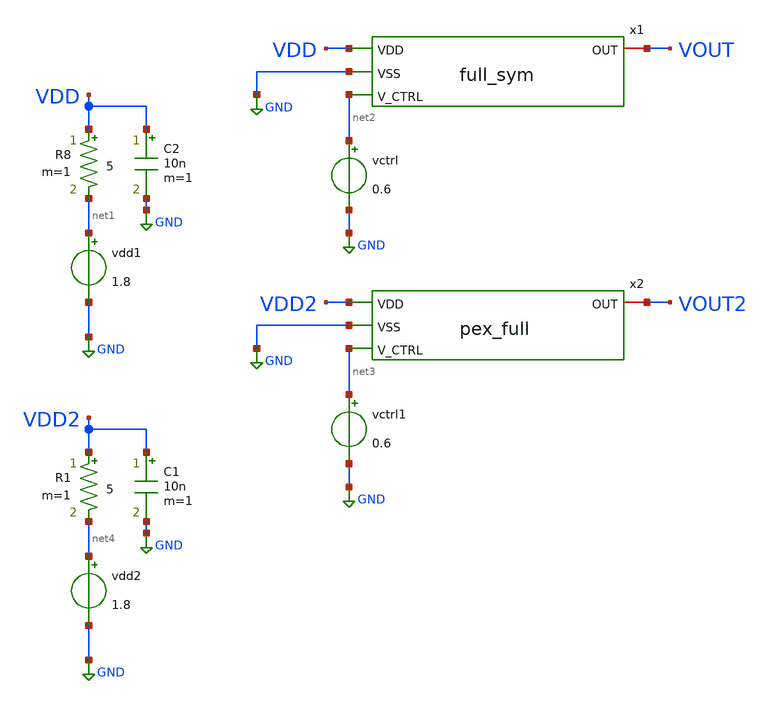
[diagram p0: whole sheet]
** sch_path: schem/sym_full_tb.sch
**.subckt sym_full_tb
vdd1 net1 GND 1.8
C2 VDD GND 10n m=1
R8 VDD net1 5 m=1
vctrl net2 GND 0.6
vctrl1 net3 GND 0.6
vdd2 net4 GND 1.8
C1 VDD2 GND 10n m=1
R1 VDD2 net4 5 m=1
x1 VDD GND VOUT net2 full_sym
x2 VDD2 GND VOUT2 net3 vco_pex
**** begin user architecture code



.include /home/zhixuan/projects/fyp_vco/magic/full/vco_pex.spice
.lib /usr/local/share/pdk/sky130A/libs.tech/ngspice/sky130.lib.spice tt

.tran 0.1n 2u
.save all

.control
    run

    meas tran t11 when VOUT=0.9 rise=2
    meas tran t21 when VOUT=0.9 rise=3

    meas tran t12 when VOUT2=0.9 rise=2
    meas tran t22 when VOUT2=0.9 rise=3

    * Calculate period and frequency from 2nd period onwards
    let period1 = t21 - t11
    let period2 = t22 - t12

    let freq1 = 1 / period1
    let freq2 = 1 / period2

    print period1
    print freq1
    print period2
    print freq2

    plot VOUT2 v(x2.comp_p_0/VIN_N)
    plot abs(i(vdd2))*1.8
    plot abs(i(vdd1))*1.8

    * echo "VOUT2 v(x2.comp_p_0/VIN_N)" > /home/zhixuan/projects/fyp_vco/schem/full_out1.txt
    * print col VOUT2 v(x2.comp_p_0/VIN_N) >> /home/zhixuan/projects/fyp_vco/schem/full_out1.txt
.endc

.end


**** end user architecture code
**.ends

* expanding   symbol:  /home/zhixuan/projects/fyp_vco/schem/full_sym.sym # of pins=4
** sym_path: schem/full_sym.sym
** sch_path: schem/full_sym.sch
.subckt full_sym VDD VSS OUT V_CTRL
*.ipin VDD
*.ipin VSS
*.iopin OUT
*.ipin V_CTRL
x1 VDD VSS high v_cap comp_n bias_n sym_comp_n
x2 VDD VSS bias_p comp_p V_CTRL v_cap sym_comp_p
x5 VDD feedback net4 VSS sym_inv
x7 VDD VSS comp_p comp_n feedback net5 sym_sr_latch
XC1 v_cap VSS sky130_fd_pr__cap_mim_m3_1 W=20 L=20 MF=1 m=1
XM33 net1 feedback VSS VSS sky130_fd_pr__nfet_01v8 L=0.3 W=2 nf=5 ad='int((5 + 1)/2) * 2 / 5 * 0.29'
+ as='int((5 + 2)/2) * 2 / 5 * 0.29' pd='2*int((5 + 1)/2) * (2 / 5 + 0.29)' ps='2*int((5 + 2)/2) * (2 / 5 + 0.29)'
+ nrd='0.29 / 2 ' nrs='0.29 / 2 ' sa=0 sb=0 sd=0 mult=1 m=1
XM34 net1 feedback VDD VDD sky130_fd_pr__pfet_01v8 L=0.3 W=2 nf=10 ad='int((10 + 1)/2) * 2 / 10 * 0.29'
+ as='int((10 + 2)/2) * 2 / 10 * 0.29' pd='2*int((10 + 1)/2) * (2 / 10 + 0.29)' ps='2*int((10 + 2)/2) * (2 / 10 + 0.29)'
+ nrd='0.29 / 2 ' nrs='0.29 / 2 ' sa=0 sb=0 sd=0 mult=1 m=1
XR1 v_cap net1 VSS sky130_fd_pr__res_xhigh_po_0p35 L=15 mult=1 m=1
x3 VDD VSS net2 net3 high bias_n sym_opamp
XR2 net2 VDD VSS sky130_fd_pr__res_xhigh_po_0p35 L=24 mult=1 m=1
XR3 VSS net2 VSS sky130_fd_pr__res_xhigh_po_0p35 L=24 mult=1 m=1
XR4 V_CTRL net3 VSS sky130_fd_pr__res_xhigh_po_0p35 L=24 mult=1 m=1
XR5 net3 high VSS sky130_fd_pr__res_xhigh_po_0p35 L=24 mult=1 m=1
XM2 OUT net4 VSS VSS sky130_fd_pr__nfet_01v8 L=0.3 W=2 nf=2 ad='int((2 + 1)/2) * 2 / 2 * 0.29' as='int((2 + 2)/2) * 2 / 2 * 0.29'
+ pd='2*int((2 + 1)/2) * (2 / 2 + 0.29)' ps='2*int((2 + 2)/2) * (2 / 2 + 0.29)' nrd='0.29 / 2 ' nrs='0.29 / 2 '
+ sa=0 sb=0 sd=0 mult=1 m=1
XM4 OUT net4 VDD VDD sky130_fd_pr__pfet_01v8 L=0.3 W=2 nf=4 ad='int((4 + 1)/2) * 2 / 4 * 0.29' as='int((4 + 2)/2) * 2 / 4 * 0.29'
+ pd='2*int((4 + 1)/2) * (2 / 4 + 0.29)' ps='2*int((4 + 2)/2) * (2 / 4 + 0.29)' nrd='0.29 / 2 ' nrs='0.29 / 2 '
+ sa=0 sb=0 sd=0 mult=1 m=1
x4 VDD VSS bias_p bias_n sym_ptat
.ends


* expanding   symbol:  /home/zhixuan/projects/fyp_vco/schem/symbol_repo/sym_comp_n.sym # of pins=6
** sym_path: schem/symbol_repo/sym_comp_n.sym
** sch_path: schem/symbol_repo/sym_comp_n.sch
.subckt sym_comp_n VDD VSS VIN_N VIN_P VOUT BIAS_N
*.ipin VDD
*.ipin VSS
*.ipin VIN_N
*.ipin VIN_P
*.ipin BIAS_N
*.iopin VOUT
XMP_diode_l net1 net1 VDD VDD sky130_fd_pr__pfet_01v8 L=0.3 W=2 nf=2 ad='int((2 + 1)/2) * 2 / 2 * 0.29'
+ as='int((2 + 2)/2) * 2 / 2 * 0.29' pd='2*int((2 + 1)/2) * (2 / 2 + 0.29)' ps='2*int((2 + 2)/2) * (2 / 2 + 0.29)'
+ nrd='0.29 / 2 ' nrs='0.29 / 2 ' sa=0 sb=0 sd=0 mult=1 m=1
XMP_cs_l net2 net1 VDD VDD sky130_fd_pr__pfet_01v8 L=0.3 W=2 nf=2 ad='int((2 + 1)/2) * 2 / 2 * 0.29'
+ as='int((2 + 2)/2) * 2 / 2 * 0.29' pd='2*int((2 + 1)/2) * (2 / 2 + 0.29)' ps='2*int((2 + 2)/2) * (2 / 2 + 0.29)'
+ nrd='0.29 / 2 ' nrs='0.29 / 2 ' sa=0 sb=0 sd=0 mult=1 m=1
XMP_cs_r net1 net2 VDD VDD sky130_fd_pr__pfet_01v8 L=0.3 W=2 nf=2 ad='int((2 + 1)/2) * 2 / 2 * 0.29'
+ as='int((2 + 2)/2) * 2 / 2 * 0.29' pd='2*int((2 + 1)/2) * (2 / 2 + 0.29)' ps='2*int((2 + 2)/2) * (2 / 2 + 0.29)'
+ nrd='0.29 / 2 ' nrs='0.29 / 2 ' sa=0 sb=0 sd=0 mult=1 m=1
XMP_diode_r net2 net2 VDD VDD sky130_fd_pr__pfet_01v8 L=0.3 W=2 nf=2 ad='int((2 + 1)/2) * 2 / 2 * 0.29'
+ as='int((2 + 2)/2) * 2 / 2 * 0.29' pd='2*int((2 + 1)/2) * (2 / 2 + 0.29)' ps='2*int((2 + 2)/2) * (2 / 2 + 0.29)'
+ nrd='0.29 / 2 ' nrs='0.29 / 2 ' sa=0 sb=0 sd=0 mult=1 m=1
XMN_vinn net1 VIN_N net3 VSS sky130_fd_pr__nfet_01v8 L=0.5 W=2.5 nf=1 ad='int((1 + 1)/2) * 2.5 / 1 * 0.29'
+ as='int((1 + 2)/2) * 2.5 / 1 * 0.29' pd='2*int((1 + 1)/2) * (2.5 / 1 + 0.29)' ps='2*int((1 + 2)/2) * (2.5 / 1 + 0.29)'
+ nrd='0.29 / 2.5 ' nrs='0.29 / 2.5 ' sa=0 sb=0 sd=0 mult=1 m=1
XMN_vinp net2 VIN_P net3 VSS sky130_fd_pr__nfet_01v8 L=0.5 W=2.5 nf=1 ad='int((1 + 1)/2) * 2.5 / 1 * 0.29'
+ as='int((1 + 2)/2) * 2.5 / 1 * 0.29' pd='2*int((1 + 1)/2) * (2.5 / 1 + 0.29)' ps='2*int((1 + 2)/2) * (2.5 / 1 + 0.29)'
+ nrd='0.29 / 2.5 ' nrs='0.29 / 2.5 ' sa=0 sb=0 sd=0 mult=1 m=1
XMN_tail net3 BIAS_N VSS VSS sky130_fd_pr__nfet_01v8 L=0.75 W=2.5 nf=2 ad='int((2 + 1)/2) * 2.5 / 2 * 0.29'
+ as='int((2 + 2)/2) * 2.5 / 2 * 0.29' pd='2*int((2 + 1)/2) * (2.5 / 2 + 0.29)' ps='2*int((2 + 2)/2) * (2.5 / 2 + 0.29)'
+ nrd='0.29 / 2.5 ' nrs='0.29 / 2.5 ' sa=0 sb=0 sd=0 mult=1 m=1
XMP_latch_r VOUT net2 VDD VDD sky130_fd_pr__pfet_01v8 L=0.15 W=0.5 nf=1 ad='int((1 + 1)/2) * 0.5 / 1 * 0.29'
+ as='int((1 + 2)/2) * 0.5 / 1 * 0.29' pd='2*int((1 + 1)/2) * (0.5 / 1 + 0.29)' ps='2*int((1 + 2)/2) * (0.5 / 1 + 0.29)'
+ nrd='0.29 / 0.5 ' nrs='0.29 / 0.5 ' sa=0 sb=0 sd=0 mult=1 m=1
XMP_latch_l net5 net1 VDD VDD sky130_fd_pr__pfet_01v8 L=0.15 W=0.5 nf=1 ad='int((1 + 1)/2) * 0.5 / 1 * 0.29'
+ as='int((1 + 2)/2) * 0.5 / 1 * 0.29' pd='2*int((1 + 1)/2) * (0.5 / 1 + 0.29)' ps='2*int((1 + 2)/2) * (0.5 / 1 + 0.29)'
+ nrd='0.29 / 0.5 ' nrs='0.29 / 0.5 ' sa=0 sb=0 sd=0 mult=1 m=1
XMN_latch_r VOUT net4 VSS VSS sky130_fd_pr__nfet_01v8 L=0.15 W=0.5 nf=1 ad='int((1 + 1)/2) * 0.5 / 1 * 0.29'
+ as='int((1 + 2)/2) * 0.5 / 1 * 0.29' pd='2*int((1 + 1)/2) * (0.5 / 1 + 0.29)' ps='2*int((1 + 2)/2) * (0.5 / 1 + 0.29)'
+ nrd='0.29 / 0.5 ' nrs='0.29 / 0.5 ' sa=0 sb=0 sd=0 mult=1 m=1
XMN_diode_l net4 net4 VSS VSS sky130_fd_pr__nfet_01v8 L=0.15 W=0.5 nf=1 ad='int((1 + 1)/2) * 0.5 / 1 * 0.29'
+ as='int((1 + 2)/2) * 0.5 / 1 * 0.29' pd='2*int((1 + 1)/2) * (0.5 / 1 + 0.29)' ps='2*int((1 + 2)/2) * (0.5 / 1 + 0.29)'
+ nrd='0.29 / 0.5 ' nrs='0.29 / 0.5 ' sa=0 sb=0 sd=0 mult=1 m=1
XMP_lim net4 net4 net5 VDD sky130_fd_pr__pfet_01v8 L=0.15 W=0.5 nf=1 ad='int((1 + 1)/2) * 0.5 / 1 * 0.29'
+ as='int((1 + 2)/2) * 0.5 / 1 * 0.29' pd='2*int((1 + 1)/2) * (0.5 / 1 + 0.29)' ps='2*int((1 + 2)/2) * (0.5 / 1 + 0.29)'
+ nrd='0.29 / 0.5 ' nrs='0.29 / 0.5 ' sa=0 sb=0 sd=0 mult=1 m=1
.ends


* expanding   symbol:  /home/zhixuan/projects/fyp_vco/schem/symbol_repo/sym_comp_p.sym # of pins=6
** sym_path: schem/symbol_repo/sym_comp_p.sym
** sch_path: schem/symbol_repo/sym_comp_p.sch
.subckt sym_comp_p VDD VSS BIAS_P VOUT VIN_P VIN_N
*.ipin VDD
*.ipin VSS
*.ipin BIAS_P
*.ipin VIN_N
*.ipin VIN_P
*.iopin VOUT
XMN_cs_l net2 net1 VSS VSS sky130_fd_pr__nfet_01v8 L=0.15 W=1 nf=1 ad='int((1 + 1)/2) * 1 / 1 * 0.29'
+ as='int((1 + 2)/2) * 1 / 1 * 0.29' pd='2*int((1 + 1)/2) * (1 / 1 + 0.29)' ps='2*int((1 + 2)/2) * (1 / 1 + 0.29)'
+ nrd='0.29 / 1 ' nrs='0.29 / 1 ' sa=0 sb=0 sd=0 mult=1 m=1
XMP_tail net4 BIAS_P VDD VDD sky130_fd_pr__pfet_01v8 L=0.75 W=2 nf=5 ad='int((5 + 1)/2) * 2 / 5 * 0.29'
+ as='int((5 + 2)/2) * 2 / 5 * 0.29' pd='2*int((5 + 1)/2) * (2 / 5 + 0.29)' ps='2*int((5 + 2)/2) * (2 / 5 + 0.29)'
+ nrd='0.29 / 2 ' nrs='0.29 / 2 ' sa=0 sb=0 sd=0 mult=1 m=1
XMP_vinn net1 VIN_N net4 VDD sky130_fd_pr__pfet_01v8 L=0.5 W=2.5 nf=2 ad='int((2 + 1)/2) * 2.5 / 2 * 0.29'
+ as='int((2 + 2)/2) * 2.5 / 2 * 0.29' pd='2*int((2 + 1)/2) * (2.5 / 2 + 0.29)' ps='2*int((2 + 2)/2) * (2.5 / 2 + 0.29)'
+ nrd='0.29 / 2.5 ' nrs='0.29 / 2.5 ' sa=0 sb=0 sd=0 mult=1 m=1
XMP_vinp net2 VIN_P net4 VDD sky130_fd_pr__pfet_01v8 L=0.5 W=2.5 nf=2 ad='int((2 + 1)/2) * 2.5 / 2 * 0.29'
+ as='int((2 + 2)/2) * 2.5 / 2 * 0.29' pd='2*int((2 + 1)/2) * (2.5 / 2 + 0.29)' ps='2*int((2 + 2)/2) * (2.5 / 2 + 0.29)'
+ nrd='0.29 / 2.5 ' nrs='0.29 / 2.5 ' sa=0 sb=0 sd=0 mult=1 m=1
XMN_diode_l net1 net1 VSS VSS sky130_fd_pr__nfet_01v8 L=0.15 W=1 nf=1 ad='int((1 + 1)/2) * 1 / 1 * 0.29'
+ as='int((1 + 2)/2) * 1 / 1 * 0.29' pd='2*int((1 + 1)/2) * (1 / 1 + 0.29)' ps='2*int((1 + 2)/2) * (1 / 1 + 0.29)'
+ nrd='0.29 / 1 ' nrs='0.29 / 1 ' sa=0 sb=0 sd=0 mult=1 m=1
XMN_diode_r net2 net2 VSS VSS sky130_fd_pr__nfet_01v8 L=0.15 W=1 nf=1 ad='int((1 + 1)/2) * 1 / 1 * 0.29'
+ as='int((1 + 2)/2) * 1 / 1 * 0.29' pd='2*int((1 + 1)/2) * (1 / 1 + 0.29)' ps='2*int((1 + 2)/2) * (1 / 1 + 0.29)'
+ nrd='0.29 / 1 ' nrs='0.29 / 1 ' sa=0 sb=0 sd=0 mult=1 m=1
XMN_cs_r net1 net2 VSS VSS sky130_fd_pr__nfet_01v8 L=0.15 W=1 nf=1 ad='int((1 + 1)/2) * 1 / 1 * 0.29'
+ as='int((1 + 2)/2) * 1 / 1 * 0.29' pd='2*int((1 + 1)/2) * (1 / 1 + 0.29)' ps='2*int((1 + 2)/2) * (1 / 1 + 0.29)'
+ nrd='0.29 / 1 ' nrs='0.29 / 1 ' sa=0 sb=0 sd=0 mult=1 m=1
XMN_latch_l net5 net1 VSS VSS sky130_fd_pr__nfet_01v8 L=0.15 W=0.5 nf=1 ad='int((1 + 1)/2) * 0.5 / 1 * 0.29'
+ as='int((1 + 2)/2) * 0.5 / 1 * 0.29' pd='2*int((1 + 1)/2) * (0.5 / 1 + 0.29)' ps='2*int((1 + 2)/2) * (0.5 / 1 + 0.29)'
+ nrd='0.29 / 0.5 ' nrs='0.29 / 0.5 ' sa=0 sb=0 sd=0 mult=1 m=1
XMN_latch_r VOUT net2 VSS VSS sky130_fd_pr__nfet_01v8 L=0.15 W=0.5 nf=1 ad='int((1 + 1)/2) * 0.5 / 1 * 0.29'
+ as='int((1 + 2)/2) * 0.5 / 1 * 0.29' pd='2*int((1 + 1)/2) * (0.5 / 1 + 0.29)' ps='2*int((1 + 2)/2) * (0.5 / 1 + 0.29)'
+ nrd='0.29 / 0.5 ' nrs='0.29 / 0.5 ' sa=0 sb=0 sd=0 mult=1 m=1
XMP_diode_l net3 net3 VDD VDD sky130_fd_pr__pfet_01v8 L=0.15 W=0.5 nf=1 ad='int((1 + 1)/2) * 0.5 / 1 * 0.29'
+ as='int((1 + 2)/2) * 0.5 / 1 * 0.29' pd='2*int((1 + 1)/2) * (0.5 / 1 + 0.29)' ps='2*int((1 + 2)/2) * (0.5 / 1 + 0.29)'
+ nrd='0.29 / 0.5 ' nrs='0.29 / 0.5 ' sa=0 sb=0 sd=0 mult=1 m=1
XMP_latch_r VOUT net3 VDD VDD sky130_fd_pr__pfet_01v8 L=0.15 W=0.5 nf=1 ad='int((1 + 1)/2) * 0.5 / 1 * 0.29'
+ as='int((1 + 2)/2) * 0.5 / 1 * 0.29' pd='2*int((1 + 1)/2) * (0.5 / 1 + 0.29)' ps='2*int((1 + 2)/2) * (0.5 / 1 + 0.29)'
+ nrd='0.29 / 0.5 ' nrs='0.29 / 0.5 ' sa=0 sb=0 sd=0 mult=1 m=1
XMP_lim net5 net5 net3 VDD sky130_fd_pr__pfet_01v8 L=0.15 W=0.5 nf=1 ad='int((1 + 1)/2) * 0.5 / 1 * 0.29'
+ as='int((1 + 2)/2) * 0.5 / 1 * 0.29' pd='2*int((1 + 1)/2) * (0.5 / 1 + 0.29)' ps='2*int((1 + 2)/2) * (0.5 / 1 + 0.29)'
+ nrd='0.29 / 0.5 ' nrs='0.29 / 0.5 ' sa=0 sb=0 sd=0 mult=1 m=1
.ends


* expanding   symbol:  /home/zhixuan/projects/fyp_vco/schem/symbol_repo/sym_inv.sym # of pins=4
** sym_path: schem/symbol_repo/sym_inv.sym
** sch_path: schem/symbol_repo/sym_inv.sch
.subckt sym_inv VDD VIN VOUT VSS
*.ipin VIN
*.ipin VDD
*.ipin VSS
*.iopin VOUT
XMN_pldwn VOUT VIN VSS VSS sky130_fd_pr__nfet_01v8 L=0.15 W=1 nf=1 ad='int((1 + 1)/2) * 1 / 1 * 0.29'
+ as='int((1 + 2)/2) * 1 / 1 * 0.29' pd='2*int((1 + 1)/2) * (1 / 1 + 0.29)' ps='2*int((1 + 2)/2) * (1 / 1 + 0.29)'
+ nrd='0.29 / 1 ' nrs='0.29 / 1 ' sa=0 sb=0 sd=0 mult=1 m=1
XMP_plup VOUT VIN VDD VDD sky130_fd_pr__pfet_01v8 L=0.15 W=2 nf=1 ad='int((1 + 1)/2) * 2 / 1 * 0.29'
+ as='int((1 + 2)/2) * 2 / 1 * 0.29' pd='2*int((1 + 1)/2) * (2 / 1 + 0.29)' ps='2*int((1 + 2)/2) * (2 / 1 + 0.29)'
+ nrd='0.29 / 2 ' nrs='0.29 / 2 ' sa=0 sb=0 sd=0 mult=1 m=1
.ends


* expanding   symbol:  /home/zhixuan/projects/fyp_vco/schem/symbol_repo/sym_sr_latch.sym # of pins=6
** sym_path: schem/symbol_repo/sym_sr_latch.sym
** sch_path: schem/symbol_repo/sym_sr_latch.sch
.subckt sym_sr_latch VDD VSS R S NEG POS
*.ipin S
*.ipin VDD
*.ipin R
*.ipin VSS
*.iopin POS
*.iopin NEG
XMN_neg POS NEG VSS VSS sky130_fd_pr__nfet_01v8 L=0.15 W=1 nf=1 ad='int((1 + 1)/2) * 1 / 1 * 0.29' as='int((1 + 2)/2) * 1 / 1 * 0.29'
+ pd='2*int((1 + 1)/2) * (1 / 1 + 0.29)' ps='2*int((1 + 2)/2) * (1 / 1 + 0.29)' nrd='0.29 / 1 ' nrs='0.29 / 1 '
+ sa=0 sb=0 sd=0 mult=1 m=1
XMP_s net1 S VDD VDD sky130_fd_pr__pfet_01v8 L=0.15 W=2 nf=1 ad='int((1 + 1)/2) * 2 / 1 * 0.29' as='int((1 + 2)/2) * 2 / 1 * 0.29'
+ pd='2*int((1 + 1)/2) * (2 / 1 + 0.29)' ps='2*int((1 + 2)/2) * (2 / 1 + 0.29)' nrd='0.29 / 2 ' nrs='0.29 / 2 '
+ sa=0 sb=0 sd=0 mult=1 m=1
XMP_neg POS NEG net1 VDD sky130_fd_pr__pfet_01v8 L=0.15 W=2 nf=1 ad='int((1 + 1)/2) * 2 / 1 * 0.29' as='int((1 + 2)/2) * 2 / 1 * 0.29'
+ pd='2*int((1 + 1)/2) * (2 / 1 + 0.29)' ps='2*int((1 + 2)/2) * (2 / 1 + 0.29)' nrd='0.29 / 2 ' nrs='0.29 / 2 '
+ sa=0 sb=0 sd=0 mult=1 m=1
XMN_s POS S VSS VSS sky130_fd_pr__nfet_01v8 L=0.15 W=1 nf=1 ad='int((1 + 1)/2) * 1 / 1 * 0.29' as='int((1 + 2)/2) * 1 / 1 * 0.29'
+ pd='2*int((1 + 1)/2) * (1 / 1 + 0.29)' ps='2*int((1 + 2)/2) * (1 / 1 + 0.29)' nrd='0.29 / 1 ' nrs='0.29 / 1 '
+ sa=0 sb=0 sd=0 mult=1 m=1
XMN_r NEG R VSS VSS sky130_fd_pr__nfet_01v8 L=0.15 W=1 nf=1 ad='int((1 + 1)/2) * 1 / 1 * 0.29' as='int((1 + 2)/2) * 1 / 1 * 0.29'
+ pd='2*int((1 + 1)/2) * (1 / 1 + 0.29)' ps='2*int((1 + 2)/2) * (1 / 1 + 0.29)' nrd='0.29 / 1 ' nrs='0.29 / 1 '
+ sa=0 sb=0 sd=0 mult=1 m=1
XMP_r net2 R VDD VDD sky130_fd_pr__pfet_01v8 L=0.15 W=2 nf=1 ad='int((1 + 1)/2) * 2 / 1 * 0.29' as='int((1 + 2)/2) * 2 / 1 * 0.29'
+ pd='2*int((1 + 1)/2) * (2 / 1 + 0.29)' ps='2*int((1 + 2)/2) * (2 / 1 + 0.29)' nrd='0.29 / 2 ' nrs='0.29 / 2 '
+ sa=0 sb=0 sd=0 mult=1 m=1
XMP_pos NEG POS net2 VDD sky130_fd_pr__pfet_01v8 L=0.15 W=2 nf=1 ad='int((1 + 1)/2) * 2 / 1 * 0.29' as='int((1 + 2)/2) * 2 / 1 * 0.29'
+ pd='2*int((1 + 1)/2) * (2 / 1 + 0.29)' ps='2*int((1 + 2)/2) * (2 / 1 + 0.29)' nrd='0.29 / 2 ' nrs='0.29 / 2 '
+ sa=0 sb=0 sd=0 mult=1 m=1
XMN_pos NEG POS VSS VSS sky130_fd_pr__nfet_01v8 L=0.15 W=1 nf=1 ad='int((1 + 1)/2) * 1 / 1 * 0.29' as='int((1 + 2)/2) * 1 / 1 * 0.29'
+ pd='2*int((1 + 1)/2) * (1 / 1 + 0.29)' ps='2*int((1 + 2)/2) * (1 / 1 + 0.29)' nrd='0.29 / 1 ' nrs='0.29 / 1 '
+ sa=0 sb=0 sd=0 mult=1 m=1
.ends


* expanding   symbol:  /home/zhixuan/projects/fyp_vco/schem/symbol_repo/sym_opamp.sym # of pins=6
** sym_path: schem/symbol_repo/sym_opamp.sym
** sch_path: schem/symbol_repo/sym_opamp.sch
.subckt sym_opamp VDD VSS VIN_P VIN_N OUT BIAS_N
*.ipin VDD
*.ipin VSS
*.ipin BIAS_N
*.iopin OUT
*.ipin VIN_N
*.ipin VIN_P
XMN_vinn net1 VIN_N net3 VSS sky130_fd_pr__nfet_01v8 L=0.5 W=1 nf=1 ad='int((1 + 1)/2) * 1 / 1 * 0.29'
+ as='int((1 + 2)/2) * 1 / 1 * 0.29' pd='2*int((1 + 1)/2) * (1 / 1 + 0.29)' ps='2*int((1 + 2)/2) * (1 / 1 + 0.29)'
+ nrd='0.29 / 1 ' nrs='0.29 / 1 ' sa=0 sb=0 sd=0 mult=1 m=1
XMP_cs_1 net2 net1 VDD VDD sky130_fd_pr__pfet_01v8 L=0.5 W=2 nf=1 ad='int((1 + 1)/2) * 2 / 1 * 0.29'
+ as='int((1 + 2)/2) * 2 / 1 * 0.29' pd='2*int((1 + 1)/2) * (2 / 1 + 0.29)' ps='2*int((1 + 2)/2) * (2 / 1 + 0.29)'
+ nrd='0.29 / 2 ' nrs='0.29 / 2 ' sa=0 sb=0 sd=0 mult=1 m=1
XMP_diode net1 net1 VDD VDD sky130_fd_pr__pfet_01v8 L=0.5 W=2 nf=1 ad='int((1 + 1)/2) * 2 / 1 * 0.29'
+ as='int((1 + 2)/2) * 2 / 1 * 0.29' pd='2*int((1 + 1)/2) * (2 / 1 + 0.29)' ps='2*int((1 + 2)/2) * (2 / 1 + 0.29)'
+ nrd='0.29 / 2 ' nrs='0.29 / 2 ' sa=0 sb=0 sd=0 mult=1 m=1
XMN_vinp net2 VIN_P net3 VSS sky130_fd_pr__nfet_01v8 L=0.5 W=1 nf=1 ad='int((1 + 1)/2) * 1 / 1 * 0.29'
+ as='int((1 + 2)/2) * 1 / 1 * 0.29' pd='2*int((1 + 1)/2) * (1 / 1 + 0.29)' ps='2*int((1 + 2)/2) * (1 / 1 + 0.29)'
+ nrd='0.29 / 1 ' nrs='0.29 / 1 ' sa=0 sb=0 sd=0 mult=1 m=1
XMN_tail_1 net3 BIAS_N VSS GND sky130_fd_pr__nfet_01v8 L=0.75 W=2 nf=1 ad='int((1 + 1)/2) * 2 / 1 * 0.29'
+ as='int((1 + 2)/2) * 2 / 1 * 0.29' pd='2*int((1 + 1)/2) * (2 / 1 + 0.29)' ps='2*int((1 + 2)/2) * (2 / 1 + 0.29)'
+ nrd='0.29 / 2 ' nrs='0.29 / 2 ' sa=0 sb=0 sd=0 mult=1 m=1
XMP_cs_2 OUT net2 VDD VDD sky130_fd_pr__pfet_01v8 L=0.5 W=2 nf=1 ad='int((1 + 1)/2) * 2 / 1 * 0.29' as='int((1 + 2)/2) * 2 / 1 * 0.29'
+ pd='2*int((1 + 1)/2) * (2 / 1 + 0.29)' ps='2*int((1 + 2)/2) * (2 / 1 + 0.29)' nrd='0.29 / 2 ' nrs='0.29 / 2 '
+ sa=0 sb=0 sd=0 mult=1 m=1
XMN_tail_2 OUT BIAS_N VSS VSS sky130_fd_pr__nfet_01v8 L=0.75 W=2 nf=1 ad='int((1 + 1)/2) * 2 / 1 * 0.29'
+ as='int((1 + 2)/2) * 2 / 1 * 0.29' pd='2*int((1 + 1)/2) * (2 / 1 + 0.29)' ps='2*int((1 + 2)/2) * (2 / 1 + 0.29)'
+ nrd='0.29 / 2 ' nrs='0.29 / 2 ' sa=0 sb=0 sd=0 mult=1 m=1
XCc net4 OUT sky130_fd_pr__cap_mim_m3_1 W=4 L=4 MF=1 m=1
XR1 net4 net2 VSS sky130_fd_pr__res_xhigh_po_0p35 L=2 mult=1 m=1
.ends


* expanding   symbol:  /home/zhixuan/projects/fyp_vco/schem/symbol_repo/sym_ptat.sym # of pins=4
** sym_path: schem/symbol_repo/sym_ptat.sym
** sch_path: schem/symbol_repo/sym_ptat.sch
.subckt sym_ptat VDD VSS BIAS_P BIAS_N
*.ipin VDD
*.ipin VSS
*.iopin BIAS_P
*.iopin BIAS_N
XMN_ptat2 net6 net1 net2 VSS sky130_fd_pr__nfet_01v8 L=0.5 W=2 nf=2 ad='int((2 + 1)/2) * 2 / 2 * 0.29'
+ as='int((2 + 2)/2) * 2 / 2 * 0.29' pd='2*int((2 + 1)/2) * (2 / 2 + 0.29)' ps='2*int((2 + 2)/2) * (2 / 2 + 0.29)'
+ nrd='0.29 / 2 ' nrs='0.29 / 2 ' sa=0 sb=0 sd=0 mult=1 m=1
XMP_diode1 net3 BIAS_P VDD VDD sky130_fd_pr__pfet_01v8 L=0.5 W=2 nf=2 ad='int((2 + 1)/2) * 2 / 2 * 0.29'
+ as='int((2 + 2)/2) * 2 / 2 * 0.29' pd='2*int((2 + 1)/2) * (2 / 2 + 0.29)' ps='2*int((2 + 2)/2) * (2 / 2 + 0.29)'
+ nrd='0.29 / 2 ' nrs='0.29 / 2 ' sa=0 sb=0 sd=0 mult=1 m=1
XMP_mir1_l net4 BIAS_P VDD VDD sky130_fd_pr__pfet_01v8 L=0.5 W=2 nf=2 ad='int((2 + 1)/2) * 2 / 2 * 0.29'
+ as='int((2 + 2)/2) * 2 / 2 * 0.29' pd='2*int((2 + 1)/2) * (2 / 2 + 0.29)' ps='2*int((2 + 2)/2) * (2 / 2 + 0.29)'
+ nrd='0.29 / 2 ' nrs='0.29 / 2 ' sa=0 sb=0 sd=0 mult=1 m=1
XMN_diode2 net5 net1 VSS VSS sky130_fd_pr__nfet_01v8 L=0.5 W=2 nf=4 ad='int((4 + 1)/2) * 2 / 4 * 0.29'
+ as='int((4 + 2)/2) * 2 / 4 * 0.29' pd='2*int((4 + 1)/2) * (2 / 4 + 0.29)' ps='2*int((4 + 2)/2) * (2 / 4 + 0.29)'
+ nrd='0.29 / 2 ' nrs='0.29 / 2 ' sa=0 sb=0 sd=0 mult=1 m=1
XMP_inv BIAS_N BIAS_P VDD VDD sky130_fd_pr__pfet_01v8 L=0.75 W=2 nf=5 ad='int((5 + 1)/2) * 2 / 5 * 0.29'
+ as='int((5 + 2)/2) * 2 / 5 * 0.29' pd='2*int((5 + 1)/2) * (2 / 5 + 0.29)' ps='2*int((5 + 2)/2) * (2 / 5 + 0.29)'
+ nrd='0.29 / 2 ' nrs='0.29 / 2 ' sa=0 sb=0 sd=0 mult=1 m=1
XMP_diode2 BIAS_P BIAS_P net3 VDD sky130_fd_pr__pfet_01v8 L=0.5 W=2 nf=2 ad='int((2 + 1)/2) * 2 / 2 * 0.29'
+ as='int((2 + 2)/2) * 2 / 2 * 0.29' pd='2*int((2 + 1)/2) * (2 / 2 + 0.29)' ps='2*int((2 + 2)/2) * (2 / 2 + 0.29)'
+ nrd='0.29 / 2 ' nrs='0.29 / 2 ' sa=0 sb=0 sd=0 mult=1 m=1
XMP_mir2_l net1 BIAS_P net4 VDD sky130_fd_pr__pfet_01v8 L=0.5 W=2 nf=2 ad='int((2 + 1)/2) * 2 / 2 * 0.29'
+ as='int((2 + 2)/2) * 2 / 2 * 0.29' pd='2*int((2 + 1)/2) * (2 / 2 + 0.29)' ps='2*int((2 + 2)/2) * (2 / 2 + 0.29)'
+ nrd='0.29 / 2 ' nrs='0.29 / 2 ' sa=0 sb=0 sd=0 mult=1 m=1
XMN_ptat1 BIAS_P net1 net6 VSS sky130_fd_pr__nfet_01v8 L=0.5 W=2 nf=2 ad='int((2 + 1)/2) * 2 / 2 * 0.29'
+ as='int((2 + 2)/2) * 2 / 2 * 0.29' pd='2*int((2 + 1)/2) * (2 / 2 + 0.29)' ps='2*int((2 + 2)/2) * (2 / 2 + 0.29)'
+ nrd='0.29 / 2 ' nrs='0.29 / 2 ' sa=0 sb=0 sd=0 mult=1 m=1
XMN_diode1 net1 net1 net5 VSS sky130_fd_pr__nfet_01v8 L=0.5 W=2 nf=4 ad='int((4 + 1)/2) * 2 / 4 * 0.29'
+ as='int((4 + 2)/2) * 2 / 4 * 0.29' pd='2*int((4 + 1)/2) * (2 / 4 + 0.29)' ps='2*int((4 + 2)/2) * (2 / 4 + 0.29)'
+ nrd='0.29 / 2 ' nrs='0.29 / 2 ' sa=0 sb=0 sd=0 mult=1 m=1
XMN_inv BIAS_N BIAS_N VSS VSS sky130_fd_pr__nfet_01v8 L=0.75 W=2.5 nf=2 ad='int((2 + 1)/2) * 2.5 / 2 * 0.29'
+ as='int((2 + 2)/2) * 2.5 / 2 * 0.29' pd='2*int((2 + 1)/2) * (2.5 / 2 + 0.29)' ps='2*int((2 + 2)/2) * (2.5 / 2 + 0.29)'
+ nrd='0.29 / 2.5 ' nrs='0.29 / 2.5 ' sa=0 sb=0 sd=0 mult=1 m=1
XR1 VSS net2 VSS sky130_fd_pr__res_xhigh_po_0p35 L=2.8 mult=1 m=1
XMP_startup net1 VSS VDD VDD sky130_fd_pr__pfet_01v8 L=13 W=1 nf=1 ad='int((1 + 1)/2) * 1 / 1 * 0.29'
+ as='int((1 + 2)/2) * 1 / 1 * 0.29' pd='2*int((1 + 1)/2) * (1 / 1 + 0.29)' ps='2*int((1 + 2)/2) * (1 / 1 + 0.29)'
+ nrd='0.29 / 1 ' nrs='0.29 / 1 ' sa=0 sb=0 sd=0 mult=1 m=1
XMN_diode3 net7 net1 VSS VSS sky130_fd_pr__nfet_01v8 L=0.5 W=2 nf=4 ad='int((4 + 1)/2) * 2 / 4 * 0.29'
+ as='int((4 + 2)/2) * 2 / 4 * 0.29' pd='2*int((4 + 1)/2) * (2 / 4 + 0.29)' ps='2*int((4 + 2)/2) * (2 / 4 + 0.29)'
+ nrd='0.29 / 2 ' nrs='0.29 / 2 ' sa=0 sb=0 sd=0 mult=1 m=1
XMN_diode4 net1 net1 net7 VSS sky130_fd_pr__nfet_01v8 L=0.5 W=2 nf=4 ad='int((4 + 1)/2) * 2 / 4 * 0.29'
+ as='int((4 + 2)/2) * 2 / 4 * 0.29' pd='2*int((4 + 1)/2) * (2 / 4 + 0.29)' ps='2*int((4 + 2)/2) * (2 / 4 + 0.29)'
+ nrd='0.29 / 2 ' nrs='0.29 / 2 ' sa=0 sb=0 sd=0 mult=1 m=1
.ends

.GLOBAL GND
.end
